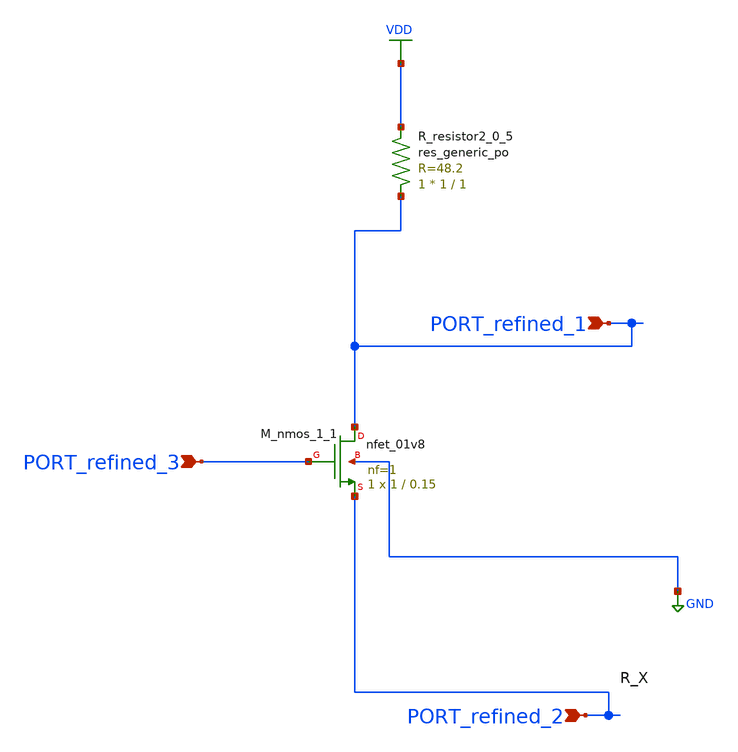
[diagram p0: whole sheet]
** sch_path: schematics/AMSNet/75.sch
**.subckt 75 PORT_refined_3 PORT_refined_1 PORT_refined_2
*.ipin PORT_refined_3
*.ipin PORT_refined_1
*.ipin PORT_refined_2
XM_nmos_1_1 PORT_refined_1 PORT_refined_3 PORT_refined_2 GND sky130_fd_pr__nfet_01v8 L=0.15 W=1 nf=1
+ ad='int((1 + 1)/2) * 1 / 1 * 0.29' as='int((1 + 2)/2) * 1 / 1 * 0.29' pd='2*int((1 + 1)/2) * (1 / 1 + 0.29)'
+ ps='2*int((1 + 2)/2) * (1 / 1 + 0.29)' nrd='0.29 / 1 ' nrs='0.29 / 1 ' sa=0 sb=0 sd=0 mult=1 m=1
XR_resistor2_0_5 PORT_refined_1 VDD sky130_fd_pr__res_generic_po W=1 L=1 m=1
**.ends
.GLOBAL GND
.GLOBAL VDD
.end
